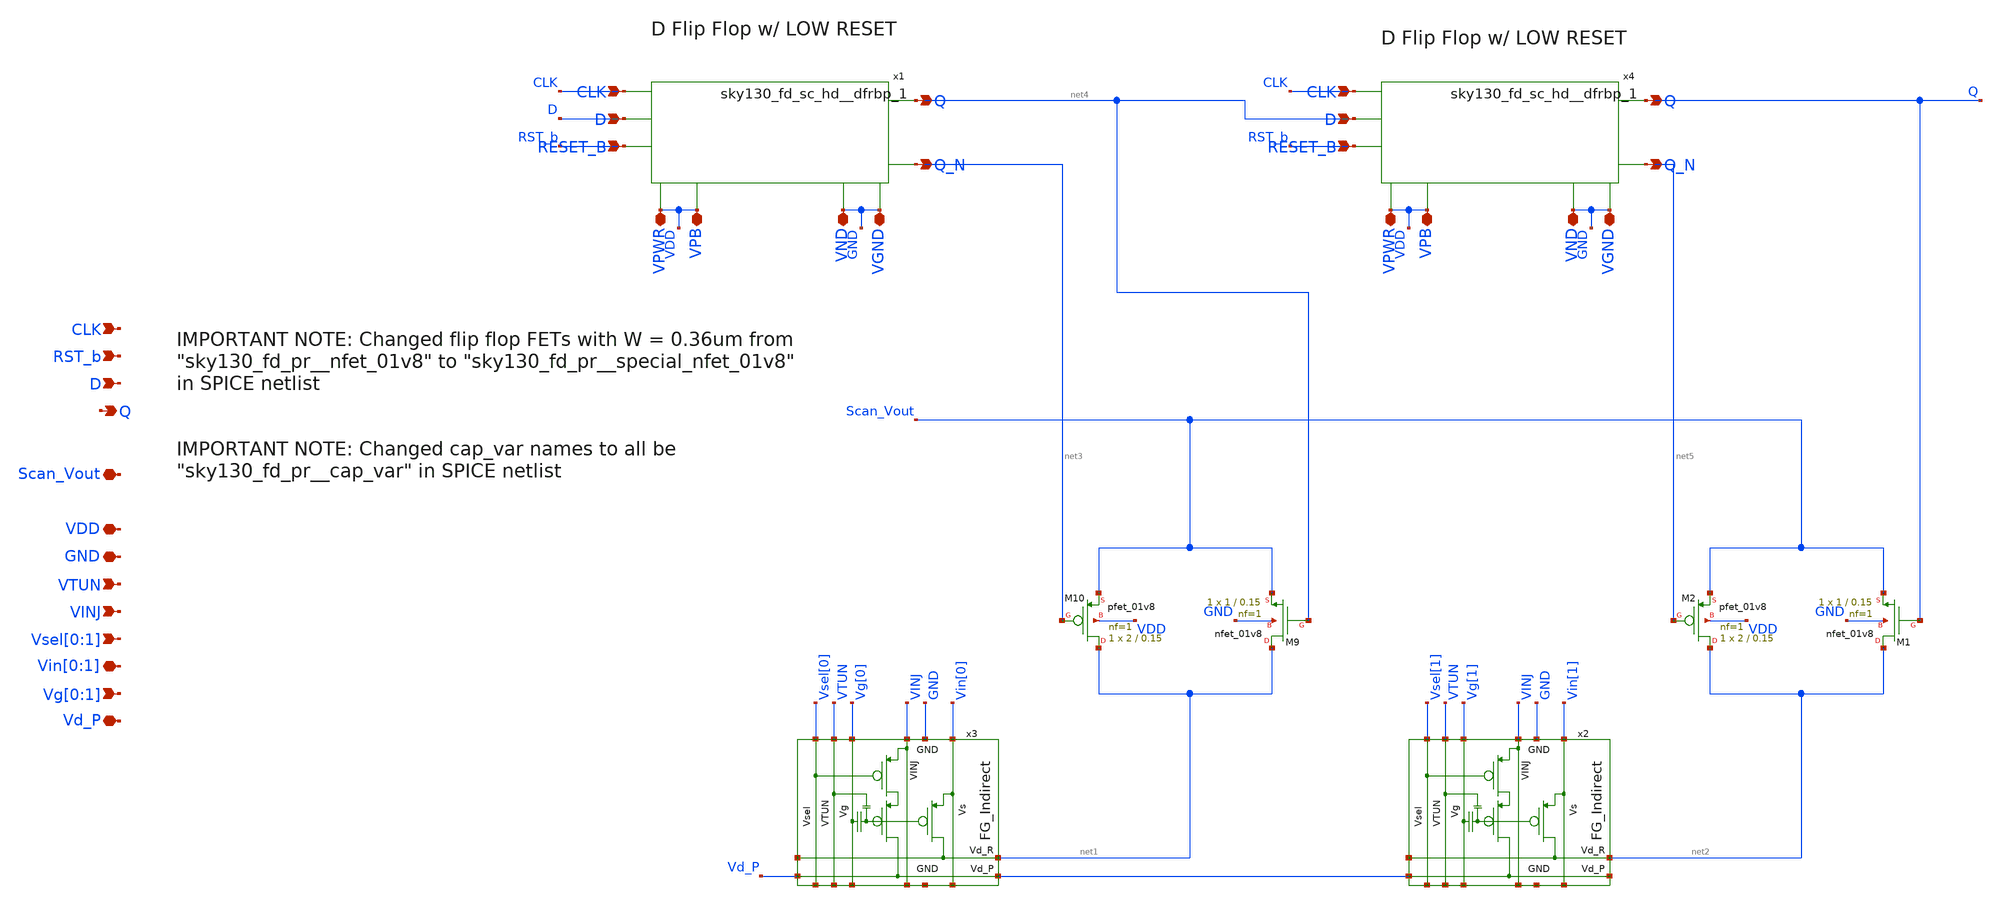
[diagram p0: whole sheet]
** sch_path: sky130_cells/Volatile_Swcs/Volatile_Swcs.sch
**.subckt Volatile_Swcs GND VDD RST_b CLK D Q Scan_Vout VTUN VINJ Vsel[0],Vsel[1] Vin[0],Vin[1]
*+ Vg[0],Vg[1] Vd_P
*.iopin GND
*.iopin VDD
*.ipin RST_b
*.ipin CLK
*.ipin D
*.opin Q
*.iopin Scan_Vout
*.ipin VTUN
*.ipin VINJ
*.ipin Vsel[0],Vsel[1]
*.iopin Vin[0],Vin[1]
*.ipin Vg[0],Vg[1]
*.iopin Vd_P
x3 Vin[0] Vg[0] Vsel[0] VTUN net1 Vd_P VINJ GND FG_Indirect
x2 Vin[1] Vg[1] Vsel[1] VTUN net2 Vd_P VINJ GND FG_Indirect
XM9 net1 net4 Scan_Vout GND sky130_fd_pr__nfet_01v8 L=0.15 W=1 nf=1 ad='int((nf+1)/2) * W/nf * 0.29'
+ as='int((nf+2)/2) * W/nf * 0.29' pd='2*int((nf+1)/2) * (W/nf + 0.29)' ps='2*int((nf+2)/2) * (W/nf + 0.29)'
+ nrd='0.29 / W' nrs='0.29 / W' sa=0 sb=0 sd=0 mult=1 m=1
XM10 net1 net3 Scan_Vout VDD sky130_fd_pr__pfet_01v8 L=0.15 W=2 nf=1 ad='int((nf+1)/2) * W/nf * 0.29'
+ as='int((nf+2)/2) * W/nf * 0.29' pd='2*int((nf+1)/2) * (W/nf + 0.29)' ps='2*int((nf+2)/2) * (W/nf + 0.29)'
+ nrd='0.29 / W' nrs='0.29 / W' sa=0 sb=0 sd=0 mult=1 m=1
XM1 net2 Q Scan_Vout GND sky130_fd_pr__nfet_01v8 L=0.15 W=1 nf=1 ad='int((nf+1)/2) * W/nf * 0.29' as='int((nf+2)/2) * W/nf * 0.29'
+ pd='2*int((nf+1)/2) * (W/nf + 0.29)' ps='2*int((nf+2)/2) * (W/nf + 0.29)' nrd='0.29 / W' nrs='0.29 / W'
+ sa=0 sb=0 sd=0 mult=1 m=1
XM2 net2 net5 Scan_Vout VDD sky130_fd_pr__pfet_01v8 L=0.15 W=2 nf=1 ad='int((nf+1)/2) * W/nf * 0.29'
+ as='int((nf+2)/2) * W/nf * 0.29' pd='2*int((nf+1)/2) * (W/nf + 0.29)' ps='2*int((nf+2)/2) * (W/nf + 0.29)'
+ nrd='0.29 / W' nrs='0.29 / W' sa=0 sb=0 sd=0 mult=1 m=1
x1 CLK D RST_b GND GND VDD VDD net4 net3 sky130_fd_sc_hd__dfrbp_1
x4 CLK net4 RST_b GND GND VDD VDD Q net5 sky130_fd_sc_hd__dfrbp_1
**** begin user architecture code

.include ../../sky130_dig_cells/flipflop/sky130_fd_sc_hd__dfrbp_1.spice

**** end user architecture code
**.ends

* expanding   symbol:  sky130_cells/Floating_Gates/Indirect/FG_Indirect.sym # of pins=16
** sym_path: sky130_cells/Floating_Gates/Indirect/FG_Indirect.sym
** sch_path: sky130_cells/Floating_Gates/Indirect/FG_Indirect.sch
.subckt FG_Indirect Vs Vg Vsel VTUN Vd_R Vd_P VINJ GND
*.iopin VINJ
*.iopin Vsel
*.iopin Vg
*.iopin Vs
*.iopin Vd_R
*.iopin Vd_P
*.iopin VTUN
*.iopin GND
XM1 Vd_R Vfg Vs VINJ sky130_fd_pr__pfet_g5v0d10v5 L=0.5 W=0.42 nf=1 ad='int((nf+1)/2) * W/nf * 0.29'
+ as='int((nf+2)/2) * W/nf * 0.29' pd='2*int((nf+1)/2) * (W/nf + 0.29)' ps='2*int((nf+2)/2) * (W/nf + 0.29)'
+ nrd='0.29 / W' nrs='0.29 / W' sa=0 sb=0 sd=0 mult=1 m=1
XM2 net1 Vsel VINJ VINJ sky130_fd_pr__pfet_g5v0d10v5 L=0.5 W=0.42 nf=1 ad='int((nf+1)/2) * W/nf * 0.29'
+ as='int((nf+2)/2) * W/nf * 0.29' pd='2*int((nf+1)/2) * (W/nf + 0.29)' ps='2*int((nf+2)/2) * (W/nf + 0.29)'
+ nrd='0.29 / W' nrs='0.29 / W' sa=0 sb=0 sd=0 mult=1 m=1
XM3 Vd_P Vfg net1 VINJ sky130_fd_pr__pfet_g5v0d10v5 L=0.5 W=0.42 nf=1 ad='int((nf+1)/2) * W/nf * 0.29'
+ as='int((nf+2)/2) * W/nf * 0.29' pd='2*int((nf+1)/2) * (W/nf + 0.29)' ps='2*int((nf+2)/2) * (W/nf + 0.29)'
+ nrd='0.29 / W' nrs='0.29 / W' sa=0 sb=0 sd=0 mult=1 m=1
XC1 Vfg VTUN GND sky130_fd_pr__cap_var_hvt W=0.29 L=0.5 VM=1 m=1
XC2 Vfg Vg GND sky130_fd_pr__cap_var_hvt W=0.54 L=0.65 VM=1 m=1
.ends

.end
